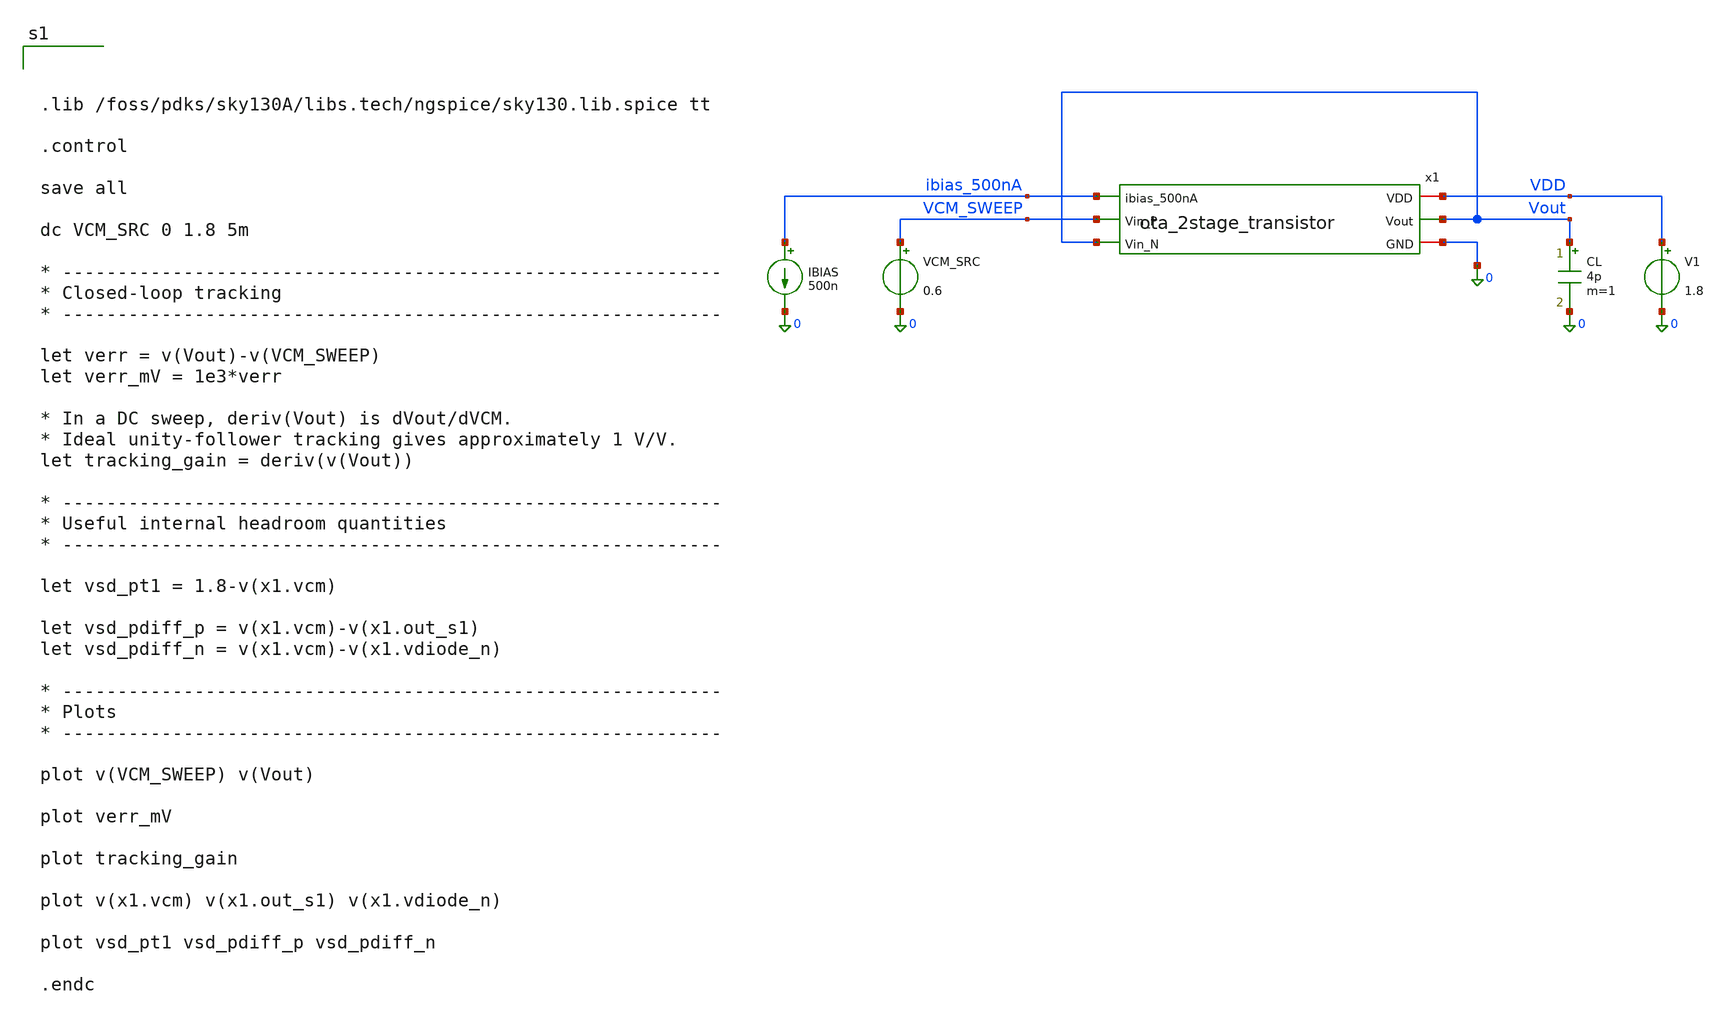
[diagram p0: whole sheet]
** sch_path: dfii/project_2stage_OTA_sim/tb_ota_2stage_icmr.sch
**.subckt tb_ota_2stage_icmr
x1 VDD ibias_500nA Vout VCM_SWEEP Vout 0 ota_2stage_transistor
V1 VDD 0 1.8
IBIAS ibias_500nA 0 500n
CL Vout 0 4p m=1
VCM_SRC VCM_SWEEP 0 0.6
**** begin user architecture code



.lib /foss/pdks/sky130A/libs.tech/ngspice/sky130.lib.spice tt

.control

save all

dc VCM_SRC 0 1.8 5m

* ------------------------------------------------------------
* Closed-loop tracking
* ------------------------------------------------------------

let verr = v(Vout)-v(VCM_SWEEP)
let verr_mV = 1e3*verr

* In a DC sweep, deriv(Vout) is dVout/dVCM.
* Ideal unity-follower tracking gives approximately 1 V/V.
let tracking_gain = deriv(v(Vout))

* ------------------------------------------------------------
* Useful internal headroom quantities
* ------------------------------------------------------------

let vsd_pt1 = 1.8-v(x1.vcm)

let vsd_pdiff_p = v(x1.vcm)-v(x1.out_s1)
let vsd_pdiff_n = v(x1.vcm)-v(x1.vdiode_n)

* ------------------------------------------------------------
* Plots
* ------------------------------------------------------------

plot v(VCM_SWEEP) v(Vout)

plot verr_mV

plot tracking_gain

plot v(x1.vcm) v(x1.out_s1) v(x1.vdiode_n)

plot vsd_pt1 vsd_pdiff_p vsd_pdiff_n

.endc



**** end user architecture code
**.ends

* expanding   symbol:
*+  /foss/designs/project_2stage_OTA/dfii/project_2stage_OTA/ota_2stage_transistor.sym # of pins=6
** sym_path: dfii/project_2stage_OTA/ota_2stage_transistor.sym
** sch_path: dfii/project_2stage_OTA/ota_2stage_transistor.sch
.subckt ota_2stage_transistor VDD ibias_500nA Vout Vin_P Vin_N GND
*.iopin VDD
*.iopin GND
*.ipin ibias_500nA
*.ipin Vin_N
*.ipin Vin_P
*.opin Vout
XNLOAD_0 vdiode_n vdiode_n GND GND sky130_fd_pr__nfet_01v8 L=12 W=3.6 nf=1 ad='int((1 + 1)/2) * 3.6 / 1 * 0.29'
+ as='int((1 + 2)/2) * 3.6 / 1 * 0.29' pd='2*int((1 + 1)/2) * (3.6 / 1 + 0.29)' ps='2*int((1 + 2)/2) * (3.6 / 1 + 0.29)'
+ nrd='0.29 / 3.6 ' nrs='0.29 / 3.6 ' sa=0 sb=0 sd=0 mult=1 m=1
XNLOAD_1 out_s1 vdiode_n GND GND sky130_fd_pr__nfet_01v8 L=12 W=3.6 nf=1 ad='int((1 + 1)/2) * 3.6 / 1 * 0.29'
+ as='int((1 + 2)/2) * 3.6 / 1 * 0.29' pd='2*int((1 + 1)/2) * (3.6 / 1 + 0.29)' ps='2*int((1 + 2)/2) * (3.6 / 1 + 0.29)'
+ nrd='0.29 / 3.6 ' nrs='0.29 / 3.6 ' sa=0 sb=0 sd=0 mult=1 m=1
XNLOAD_2 Vout out_s1 GND GND sky130_fd_pr__nfet_01v8 L=2 W=3.6 nf=1 ad='int((1 + 1)/2) * 3.6 / 1 * 0.29'
+ as='int((1 + 2)/2) * 3.6 / 1 * 0.29' pd='2*int((1 + 1)/2) * (3.6 / 1 + 0.29)' ps='2*int((1 + 2)/2) * (3.6 / 1 + 0.29)'
+ nrd='0.29 / 3.6 ' nrs='0.29 / 3.6 ' sa=0 sb=0 sd=0 mult=2 m=2
XPDIFF_N vdiode_n Vin_N VCM VCM sky130_fd_pr__pfet_01v8 L=1 W=7.4 nf=1 ad='int((1 + 1)/2) * 7.4 / 1 * 0.29'
+ as='int((1 + 2)/2) * 7.4 / 1 * 0.29' pd='2*int((1 + 1)/2) * (7.4 / 1 + 0.29)' ps='2*int((1 + 2)/2) * (7.4 / 1 + 0.29)'
+ nrd='0.29 / 7.4 ' nrs='0.29 / 7.4 ' sa=0 sb=0 sd=0 mult=12 m=12
XPDIFF_P out_s1 Vin_P VCM VCM sky130_fd_pr__pfet_01v8 L=1 W=7.4 nf=1 ad='int((1 + 1)/2) * 7.4 / 1 * 0.29'
+ as='int((1 + 2)/2) * 7.4 / 1 * 0.29' pd='2*int((1 + 1)/2) * (7.4 / 1 + 0.29)' ps='2*int((1 + 2)/2) * (7.4 / 1 + 0.29)'
+ nrd='0.29 / 7.4 ' nrs='0.29 / 7.4 ' sa=0 sb=0 sd=0 mult=12 m=12
XPTAIL_1 VCM ibias_500nA VDD VDD sky130_fd_pr__pfet_01v8 L=1 W=1.76 nf=1 ad='int((1 + 1)/2) * 1.76 / 1 * 0.29'
+ as='int((1 + 2)/2) * 1.76 / 1 * 0.29' pd='2*int((1 + 1)/2) * (1.76 / 1 + 0.29)' ps='2*int((1 + 2)/2) * (1.76 / 1 + 0.29)'
+ nrd='0.29 / 1.76 ' nrs='0.29 / 1.76 ' sa=0 sb=0 sd=0 mult=1 m=1
XPTAIL_2 Vout ibias_500nA VDD VDD sky130_fd_pr__pfet_01v8 L=1 W=1.76 nf=1 ad='int((1 + 1)/2) * 1.76 / 1 * 0.29'
+ as='int((1 + 2)/2) * 1.76 / 1 * 0.29' pd='2*int((1 + 1)/2) * (1.76 / 1 + 0.29)' ps='2*int((1 + 2)/2) * (1.76 / 1 + 0.29)'
+ nrd='0.29 / 1.76 ' nrs='0.29 / 1.76 ' sa=0 sb=0 sd=0 mult=6 m=6
XPTAIL_0 ibias_500nA ibias_500nA VDD VDD sky130_fd_pr__pfet_01v8 L=1 W=1.76 nf=1 ad='int((1 + 1)/2) * 1.76 / 1 * 0.29'
+ as='int((1 + 2)/2) * 1.76 / 1 * 0.29' pd='2*int((1 + 1)/2) * (1.76 / 1 + 0.29)' ps='2*int((1 + 2)/2) * (1.76 / 1 + 0.29)'
+ nrd='0.29 / 1.76 ' nrs='0.29 / 1.76 ' sa=0 sb=0 sd=0 mult=1 m=1
XCMILLER out_s1 net1 sky130_fd_pr__cap_mim_m3_1 W=19 L=19 MF=1 m=1
XRMILLER Vout net1 GND sky130_fd_pr__res_xhigh_po_0p35 L=31.5 mult=1 m=1
.ends

.GLOBAL VDD
.end
